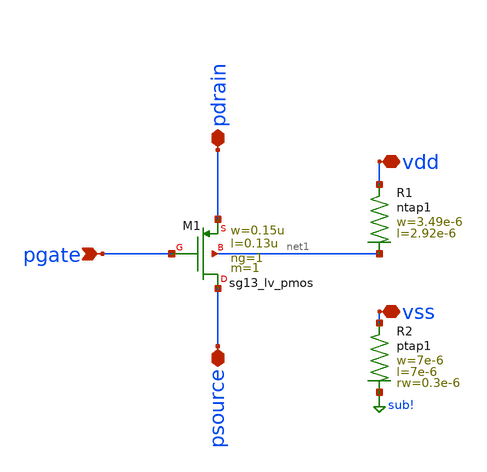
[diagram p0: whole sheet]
** sch_path: ihp-sg13g2/libs.tech/klayout/sg13g2_tests/lvs_testcases/pmos_test.sch
**.subckt pmos_test vdd pgate pdrain psource vss
*.iopin vdd
*.ipin pgate
*.iopin pdrain
*.iopin psource
*.iopin vss
XM1 psource pgate pdrain net1 sg13_lv_pmos w=0.15u l=0.13u ng=1 m=1 mm_ok=1
XR1 vdd net1 ntap1 R=19.61 w=3.49e-6 l=2.92e-6
XR2 vss sub! ptap1 R=8.504 w=7e-6 l=7e-6
**.ends
.GLOBAL sub!
.end
